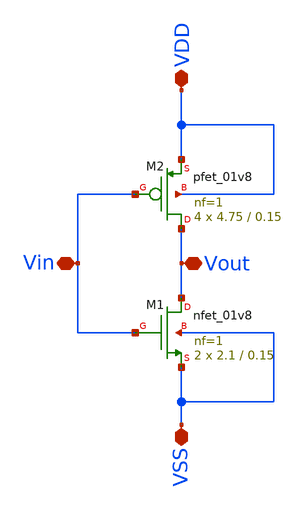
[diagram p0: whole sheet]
** sch_path: TT/inverter_RO_rel.sch
**.subckt inverter_RO_rel VDD VSS Vin Vout
*.iopin VDD
*.iopin VSS
*.iopin Vin
*.iopin Vout
XM2 Vout Vin VDD VDD sky130_fd_pr__pfet_01v8 L=0.15 W=4.75 nf=1 ad='int((nf+1)/2) * W/nf * 0.29' as='int((nf+2)/2) * W/nf * 0.29'
+ pd='2*int((nf+1)/2) * (W/nf + 0.29)' ps='2*int((nf+2)/2) * (W/nf + 0.29)' nrd='0.29 / W' nrs='0.29 / W'
+ sa=0 sb=0 sd=0 mult=4 m=4
XM1 Vout Vin VSS VSS sky130_fd_pr__nfet_01v8 L=0.15 W=2.1 nf=1 ad='int((nf+1)/2) * W/nf * 0.29' as='int((nf+2)/2) * W/nf * 0.29'
+ pd='2*int((nf+1)/2) * (W/nf + 0.29)' ps='2*int((nf+2)/2) * (W/nf + 0.29)' nrd='0.29 / W' nrs='0.29 / W'
+ sa=0 sb=0 sd=0 mult=2 m=2
**.ends
.end
